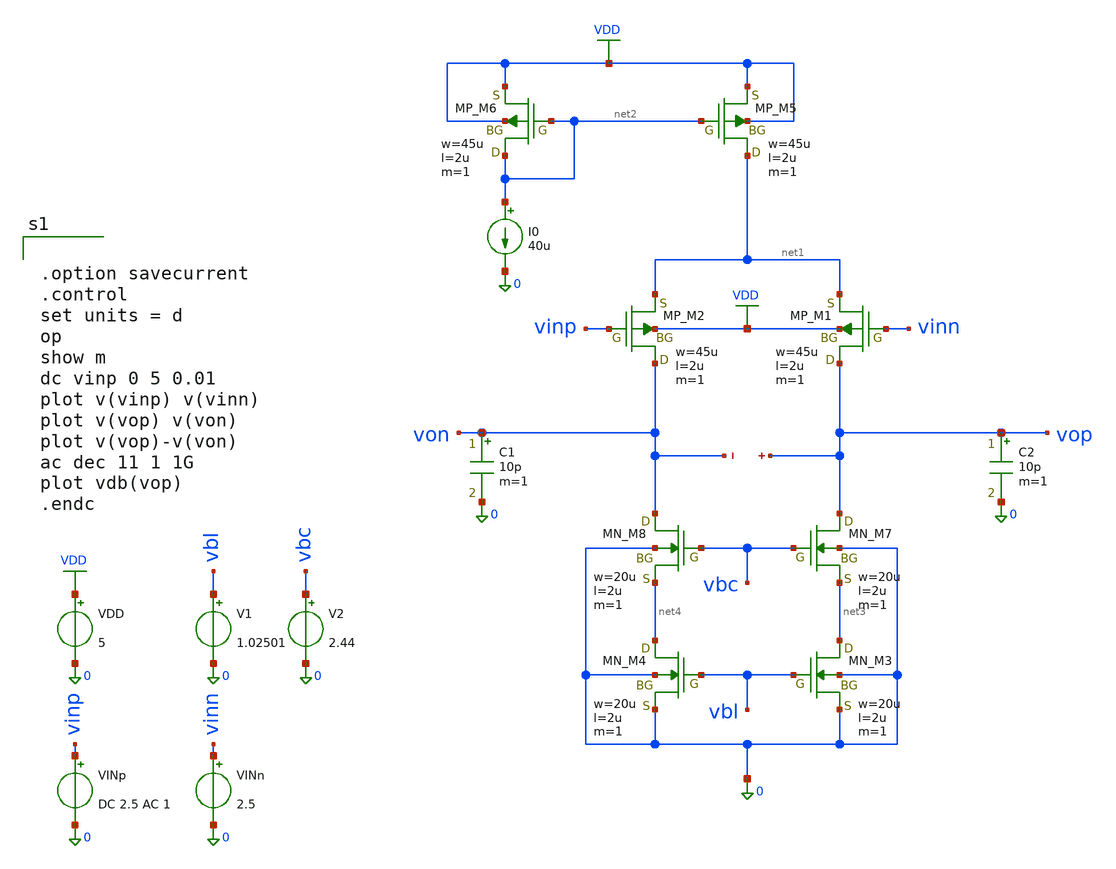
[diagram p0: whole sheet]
** sch_path: member_project/JJY_Receiver/Masahiro/jjy_recv/diff_amp/diff_cascode.sch
**.subckt diff_cascode
VDD VDD 0 5
VINp vinp 0 DC 2.5 AC 1
I0 net2 0 40u
C1 von 0 10p m=1
V1 vbl 0 1.02501
XM1 vop vinn net1 VDD PMOS w=45u l=2u as=0 ad=0 ps=0 pd=0 nrd=0 nrs=0 m=1
XM2 von vinp net1 VDD PMOS w=45u l=2u as=0 ad=0 ps=0 pd=0 nrd=0 nrs=0 m=1
XM3 net3 vbl 0 0 NMOS w=20u l=2u as=0 ad=0 ps=0 pd=0 nrd=0 nrs=0 m=1
XM4 net4 vbl 0 0 NMOS w=20u l=2u as=0 ad=0 ps=0 pd=0 nrd=0 nrs=0 m=1
XM5 net1 net2 VDD VDD PMOS w=45u l=2u as=0 ad=0 ps=0 pd=0 nrd=0 nrs=0 m=1
XM6 net2 net2 VDD VDD PMOS w=45u l=2u as=0 ad=0 ps=0 pd=0 nrd=0 nrs=0 m=1
C2 vop 0 10p m=1
VINn vinn 0 2.5
XM7 vop vbc net3 0 NMOS w=20u l=2u as=0 ad=0 ps=0 pd=0 nrd=0 nrs=0 m=1
XM8 von vbc net4 0 NMOS w=20u l=2u as=0 ad=0 ps=0 pd=0 nrd=0 nrs=0 m=1
V2 vbc 0 2.44
.save v(vop)
.save v(von)
**** begin user architecture code
 .include $::LIB/ip62_models


.option savecurrent
.control
set units = d
op
show m
dc vinp 0 5 0.01
plot v(vinp) v(vinn)
plot v(vop) v(von)
plot v(vop)-v(von)
ac dec 11 1 1G
plot vdb(vop)
.endc


**** end user architecture code
**.ends
.GLOBAL VDD
.end
